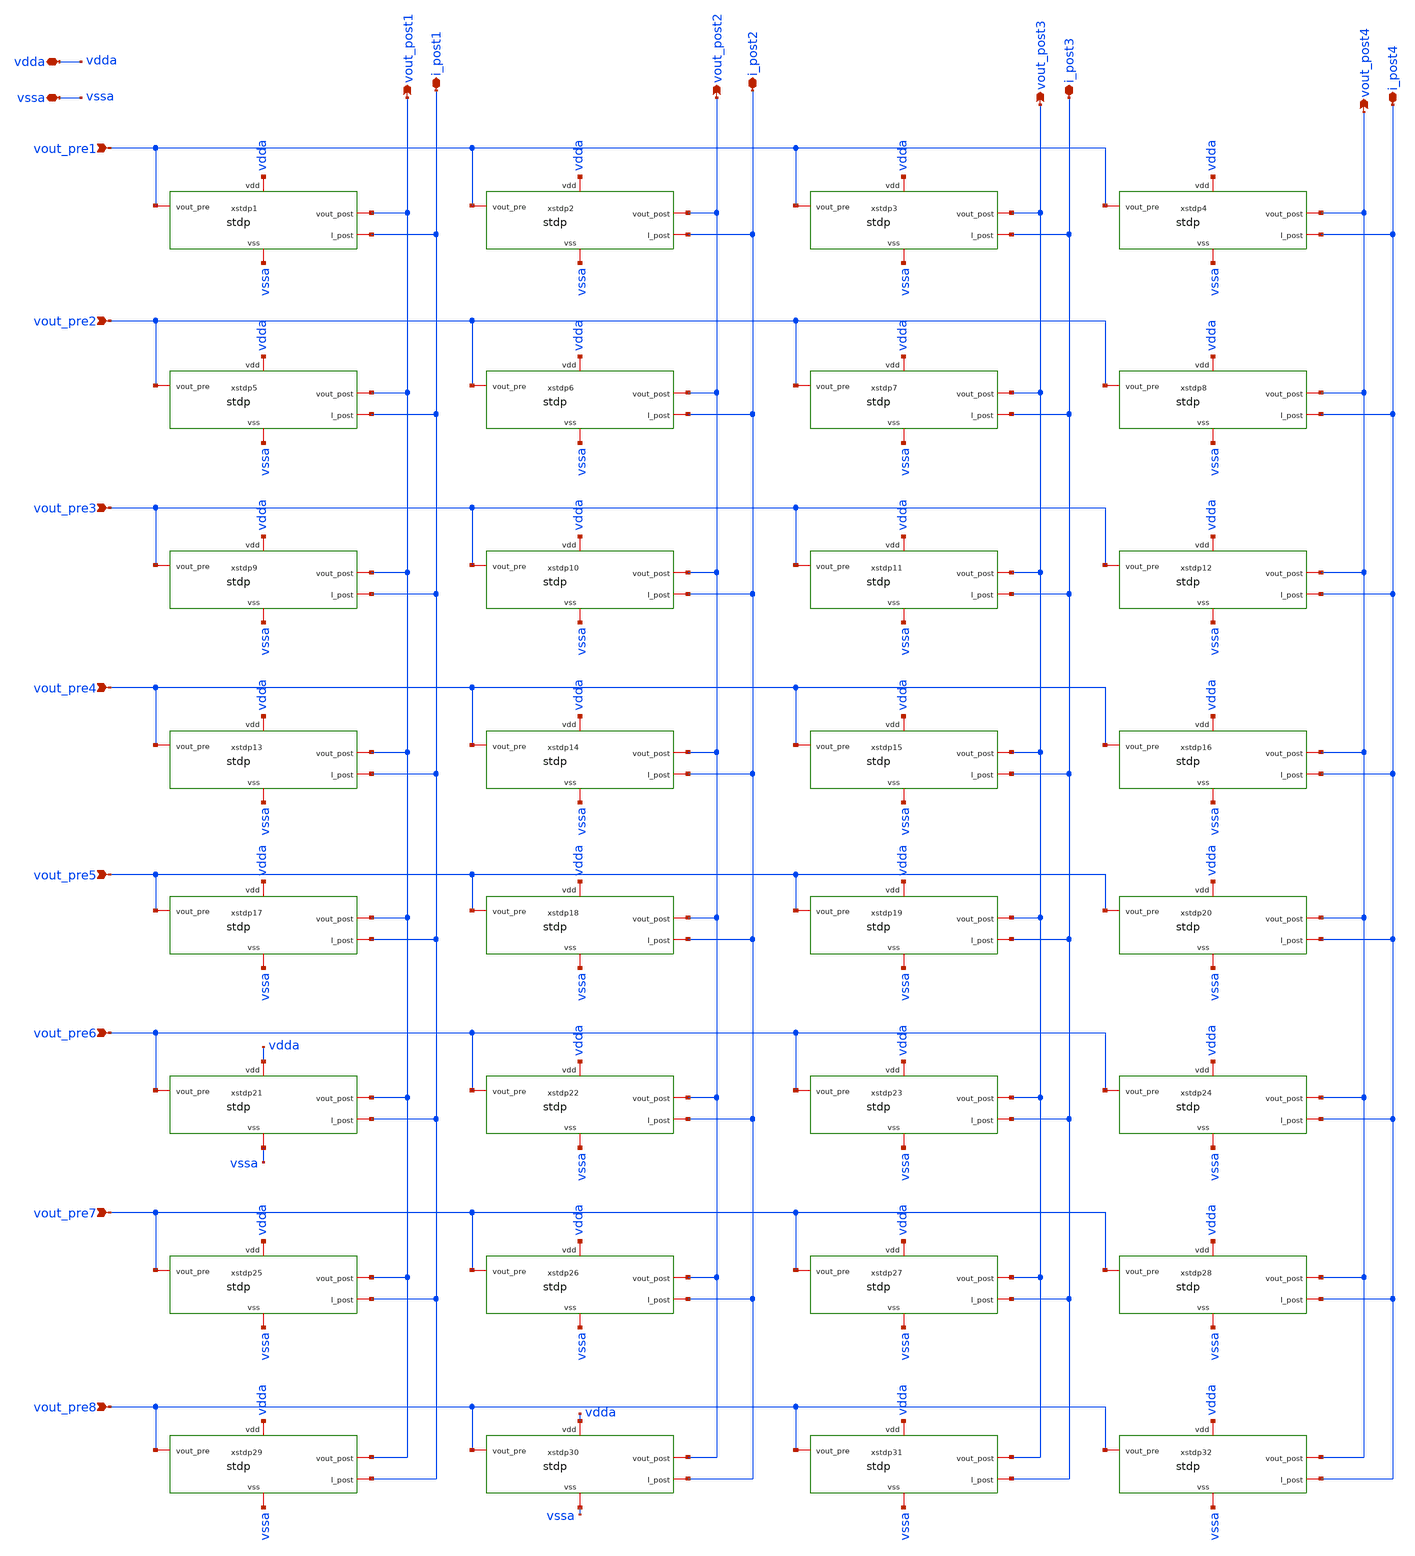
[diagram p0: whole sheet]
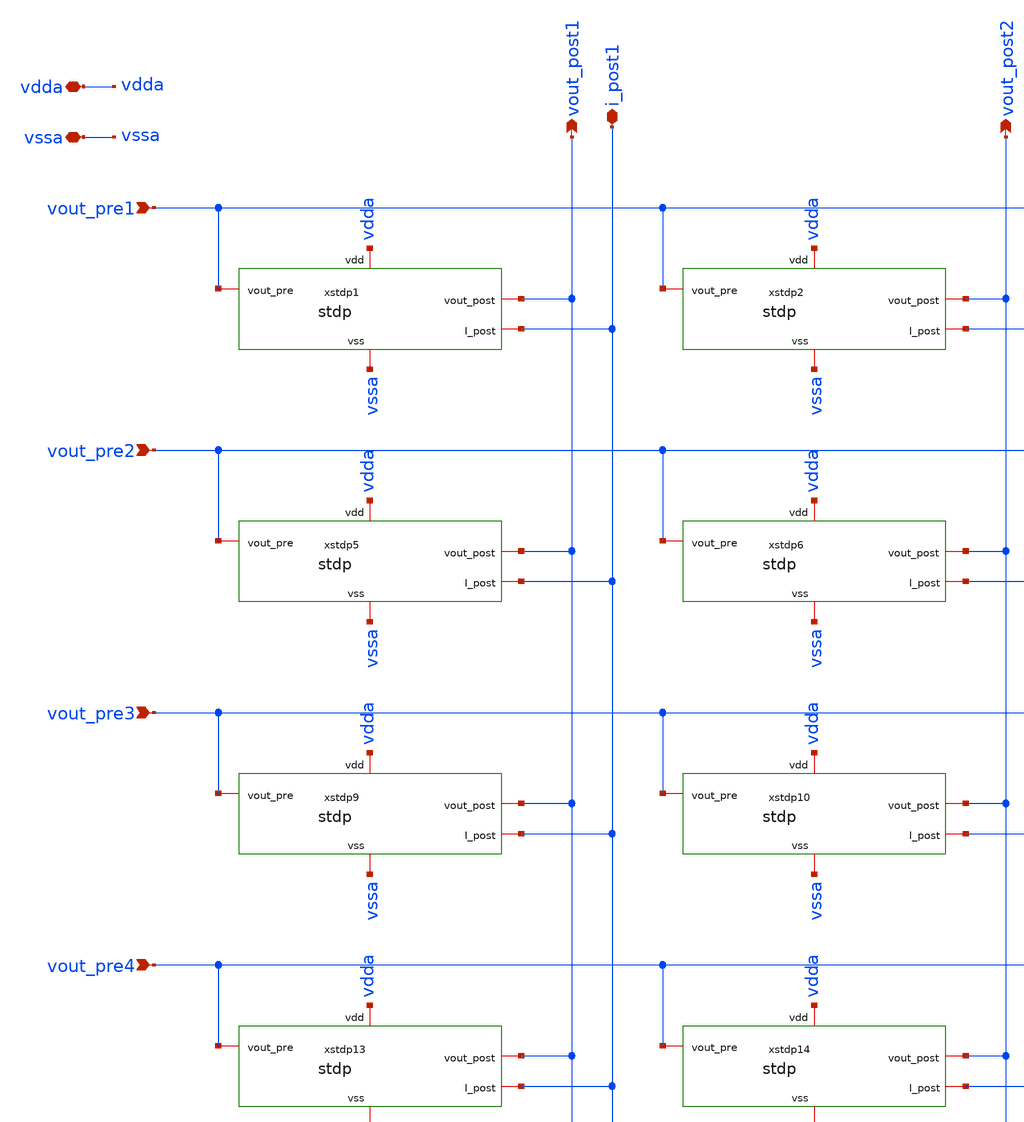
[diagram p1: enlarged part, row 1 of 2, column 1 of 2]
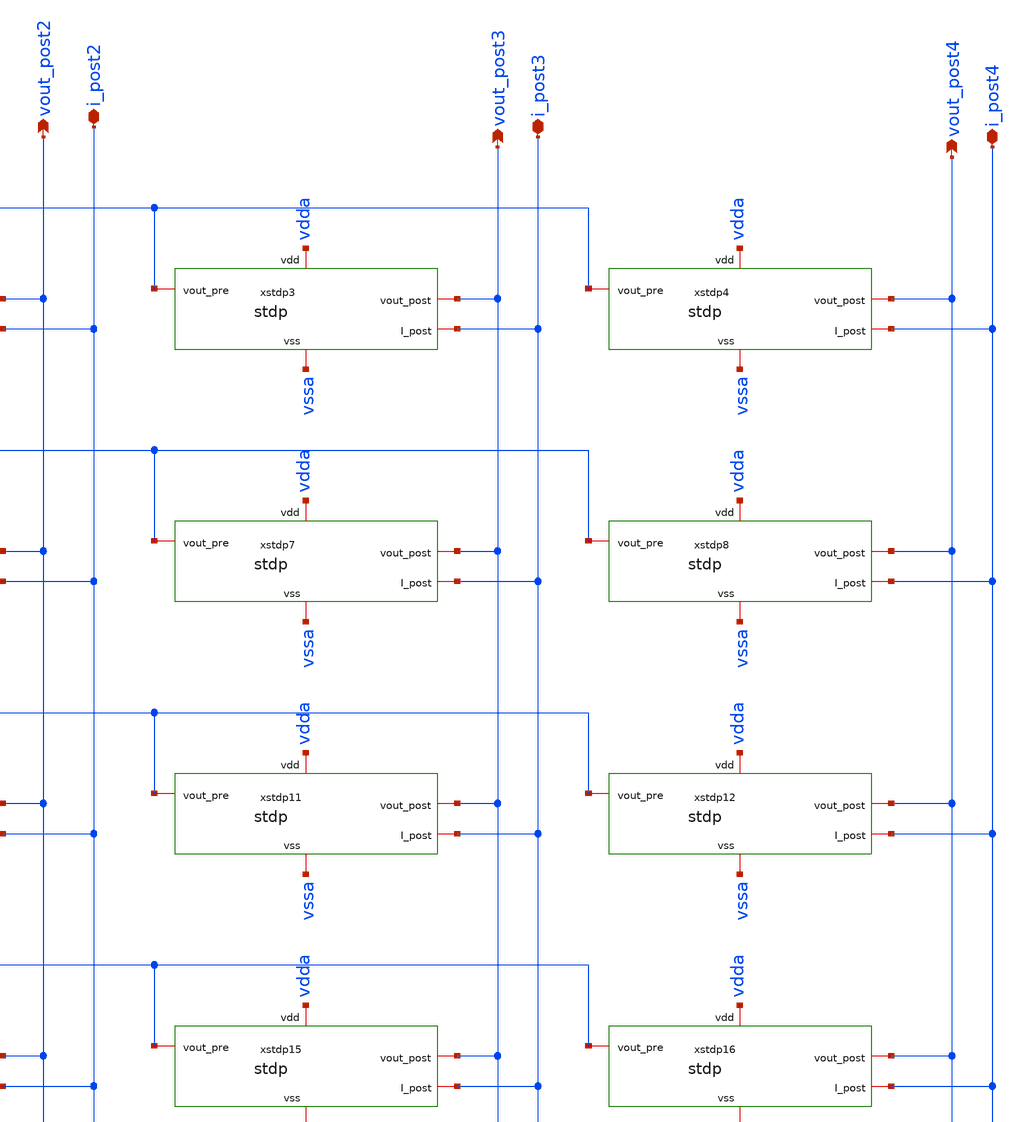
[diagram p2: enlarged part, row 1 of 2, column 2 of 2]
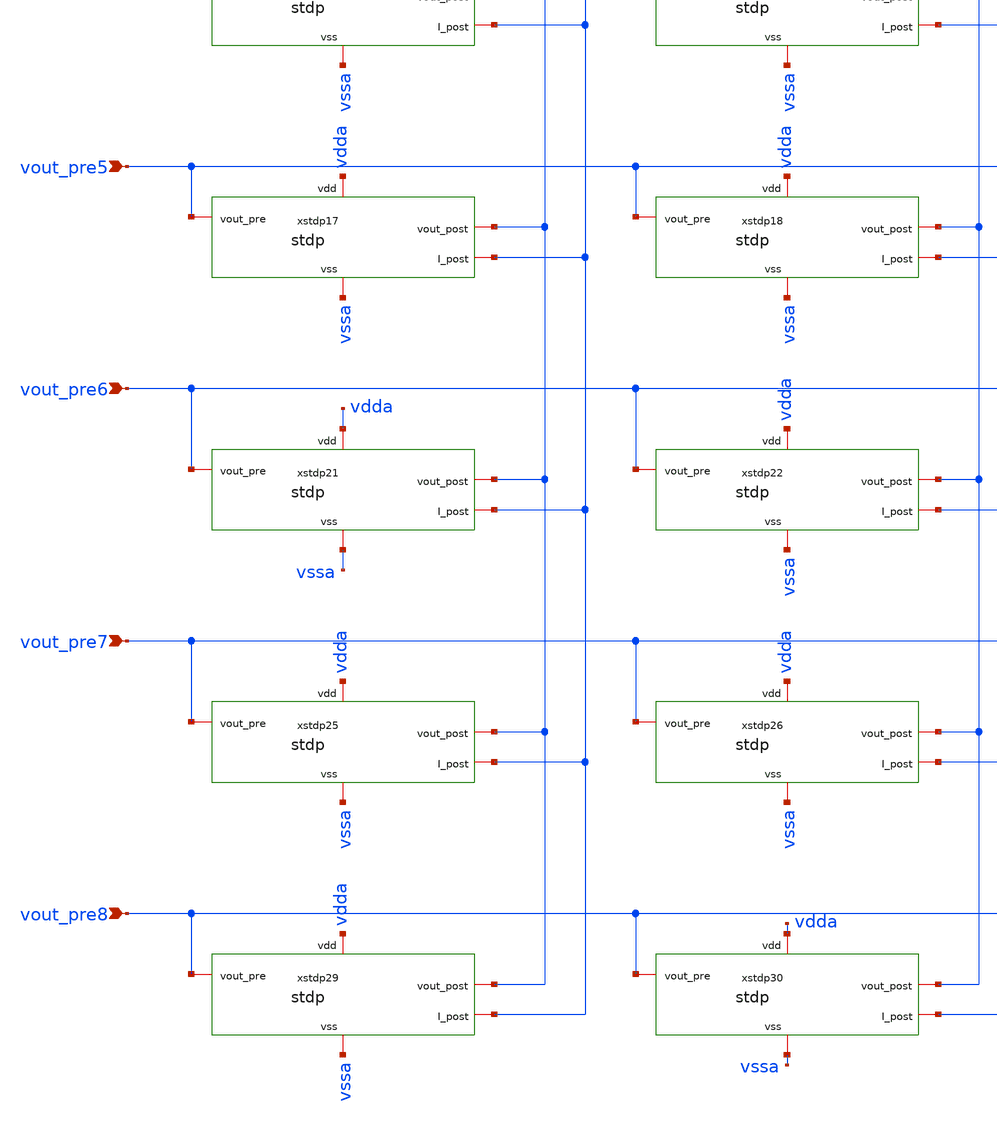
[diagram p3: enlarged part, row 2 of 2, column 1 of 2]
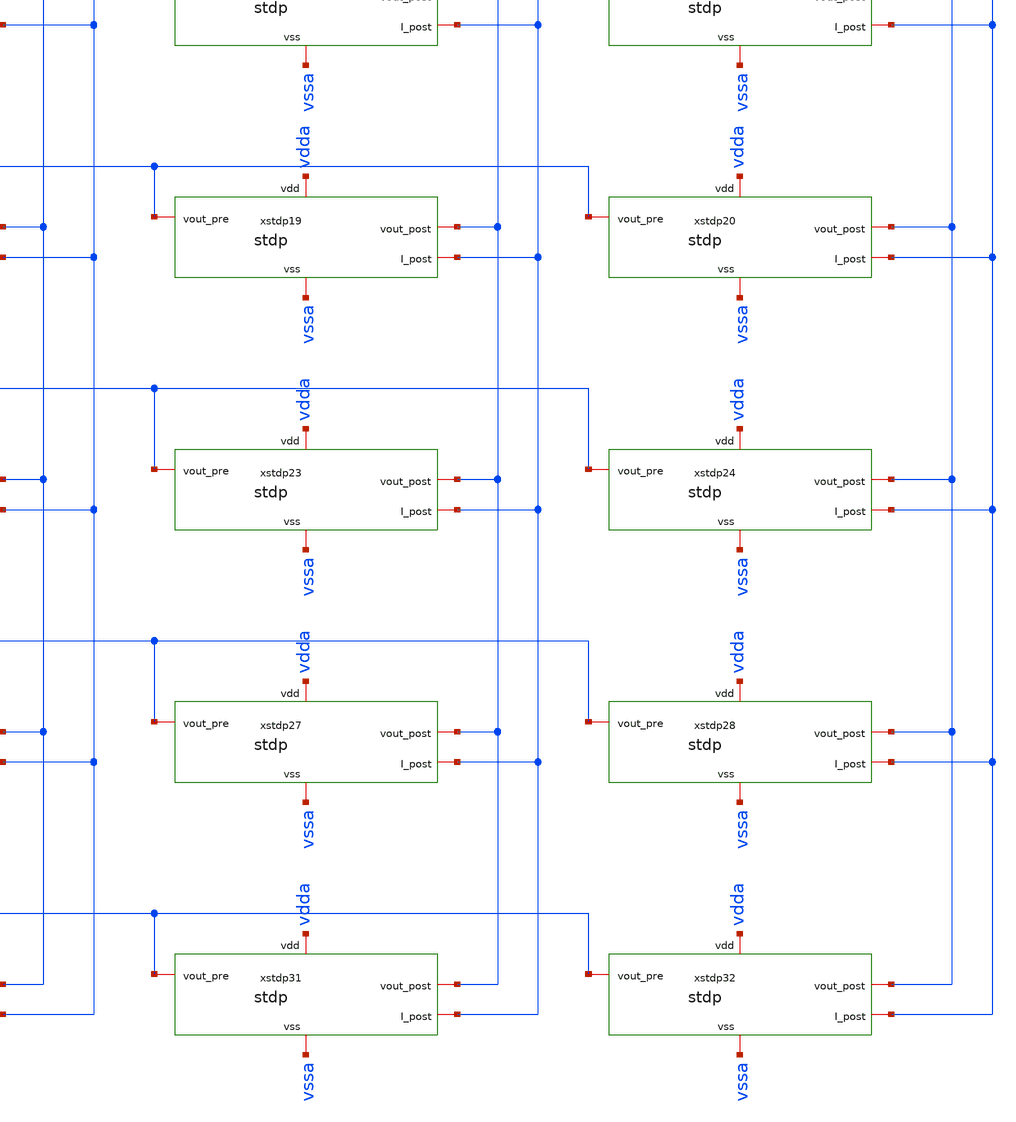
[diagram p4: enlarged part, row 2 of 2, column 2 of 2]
** sch_path: Synapse/stdp_8x4.sch
**.subckt stdp_8x4 vout_pre1 vout_post1 vdda vssa i_post1 i_post3 i_post4 vout_pre2 vout_pre3
*+ vout_pre4 vout_post2 vout_post3 vout_post4 i_post2 vout_pre5 vout_pre6 vout_pre7 vout_pre8
*.ipin vout_pre1
*.opin vout_post1
*.iopin vdda
*.iopin vssa
*.iopin i_post1
*.iopin i_post3
*.iopin i_post4
*.ipin vout_pre2
*.ipin vout_pre3
*.ipin vout_pre4
*.opin vout_post2
*.opin vout_post3
*.opin vout_post4
*.iopin i_post2
*.ipin vout_pre5
*.ipin vout_pre6
*.ipin vout_pre7
*.ipin vout_pre8
xstdp2 vdda vssa vout_pre1 vout_post2 i_post2 stdp
xstdp3 vdda vssa vout_pre1 vout_post3 i_post3 stdp
xstdp4 vdda vssa vout_pre1 vout_post4 i_post4 stdp
xstdp5 vdda vssa vout_pre2 vout_post1 i_post1 stdp
xstdp6 vdda vssa vout_pre2 vout_post2 i_post2 stdp
xstdp7 vdda vssa vout_pre2 vout_post3 i_post3 stdp
xstdp8 vdda vssa vout_pre2 vout_post4 i_post4 stdp
xstdp9 vdda vssa vout_pre3 vout_post1 i_post1 stdp
xstdp10 vdda vssa vout_pre3 vout_post2 i_post2 stdp
xstdp11 vdda vssa vout_pre3 vout_post3 i_post3 stdp
xstdp12 vdda vssa vout_pre3 vout_post4 i_post4 stdp
xstdp13 vdda vssa vout_pre4 vout_post1 i_post1 stdp
xstdp14 vdda vssa vout_pre4 vout_post2 i_post2 stdp
xstdp15 vdda vssa vout_pre4 vout_post3 i_post3 stdp
xstdp16 vdda vssa vout_pre4 vout_post4 i_post4 stdp
xstdp17 vdda vssa vout_pre5 vout_post1 i_post1 stdp
xstdp18 vdda vssa vout_pre5 vout_post2 i_post2 stdp
xstdp19 vdda vssa vout_pre5 vout_post3 i_post3 stdp
xstdp20 vdda vssa vout_pre5 vout_post4 i_post4 stdp
xstdp21 vdda vssa vout_pre6 vout_post1 i_post1 stdp
xstdp22 vdda vssa vout_pre6 vout_post2 i_post2 stdp
xstdp23 vdda vssa vout_pre6 vout_post3 i_post3 stdp
xstdp24 vdda vssa vout_pre6 vout_post4 i_post4 stdp
xstdp25 vdda vssa vout_pre7 vout_post1 i_post1 stdp
xstdp26 vdda vssa vout_pre7 vout_post2 i_post2 stdp
xstdp27 vdda vssa vout_pre7 vout_post3 i_post3 stdp
xstdp28 vdda vssa vout_pre7 vout_post4 i_post4 stdp
xstdp29 vdda vssa vout_pre8 vout_post1 i_post1 stdp
xstdp30 vdda vssa vout_pre8 vout_post2 i_post2 stdp
xstdp31 vdda vssa vout_pre8 vout_post3 i_post3 stdp
xstdp32 vdda vssa vout_pre8 vout_post4 i_post4 stdp
xstdp1 vdda vssa vout_pre1 vout_post1 i_post1 stdp
**.ends

* expanding   symbol:  Synapse/stdp.sym # of pins=5
** sym_path: Synapse/stdp.sym
** sch_path: Synapse/stdp.sch
.subckt stdp vdd vss vout_pre vout_post I_post
*.iopin vdd
*.iopin vss
*.iopin vout_post
*.iopin vout_pre
*.iopin I_post
XM2 A vout_pre te vss sky130_fd_pr__nfet_01v8 L=0.15 W=7.5 nf=1 ad='int((nf+1)/2) * W/nf * 0.29' as='int((nf+2)/2) * W/nf * 0.29'
+ pd='2*int((nf+1)/2) * (W/nf + 0.29)' ps='2*int((nf+2)/2) * (W/nf + 0.29)' nrd='0.29 / W' nrs='0.29 / W'
+ sa=0 sb=0 sd=0 mult=1 m=1
XM3 te vout_post vss vss sky130_fd_pr__nfet_01v8 L=0.15 W=7.5 nf=1 ad='int((nf+1)/2) * W/nf * 0.29' as='int((nf+2)/2) * W/nf * 0.29'
+ pd='2*int((nf+1)/2) * (W/nf + 0.29)' ps='2*int((nf+2)/2) * (W/nf + 0.29)' nrd='0.29 / W' nrs='0.29 / W'
+ sa=0 sb=0 sd=0 mult=1 m=1
XM4 net1 vout_pre vss vss sky130_fd_pr__nfet_01v8 L=0.15 W=7.5 nf=1 ad='int((nf+1)/2) * W/nf * 0.29'
+ as='int((nf+2)/2) * W/nf * 0.29' pd='2*int((nf+1)/2) * (W/nf + 0.29)' ps='2*int((nf+2)/2) * (W/nf + 0.29)'
+ nrd='0.29 / W' nrs='0.29 / W' sa=0 sb=0 sd=0 mult=1 m=1
XR2 te be rram_v0
XM14 I_post A vdd vdd sky130_fd_pr__pfet_01v8 L=30 W=0.5 nf=1 ad='int((nf+1)/2) * W/nf * 0.29' as='int((nf+2)/2) * W/nf * 0.29'
+ pd='2*int((nf+1)/2) * (W/nf + 0.29)' ps='2*int((nf+2)/2) * (W/nf + 0.29)' nrd='0.29 / W' nrs='0.29 / W'
+ sa=0 sb=0 sd=0 mult=1 m=1
XM15 A A vdd vdd sky130_fd_pr__pfet_01v8 L=0.15 W=2.5 nf=1 ad='int((nf+1)/2) * W/nf * 0.29' as='int((nf+2)/2) * W/nf * 0.29'
+ pd='2*int((nf+1)/2) * (W/nf + 0.29)' ps='2*int((nf+2)/2) * (W/nf + 0.29)' nrd='0.29 / W' nrs='0.29 / W'
+ sa=0 sb=0 sd=0 mult=1 m=1
**** begin user architecture code


.save v(te) v(be) i(vmr)


**** end user architecture code
Vmr be net1 0
.save i(vmr)
XM1 A vout_post net1 vss sky130_fd_pr__nfet_01v8 L=0.15 W=7.5 nf=1 ad='int((nf+1)/2) * W/nf * 0.29' as='int((nf+2)/2) * W/nf * 0.29'
+ pd='2*int((nf+1)/2) * (W/nf + 0.29)' ps='2*int((nf+2)/2) * (W/nf + 0.29)' nrd='0.29 / W' nrs='0.29 / W'
+ sa=0 sb=0 sd=0 mult=1 m=1
.ends

.end
